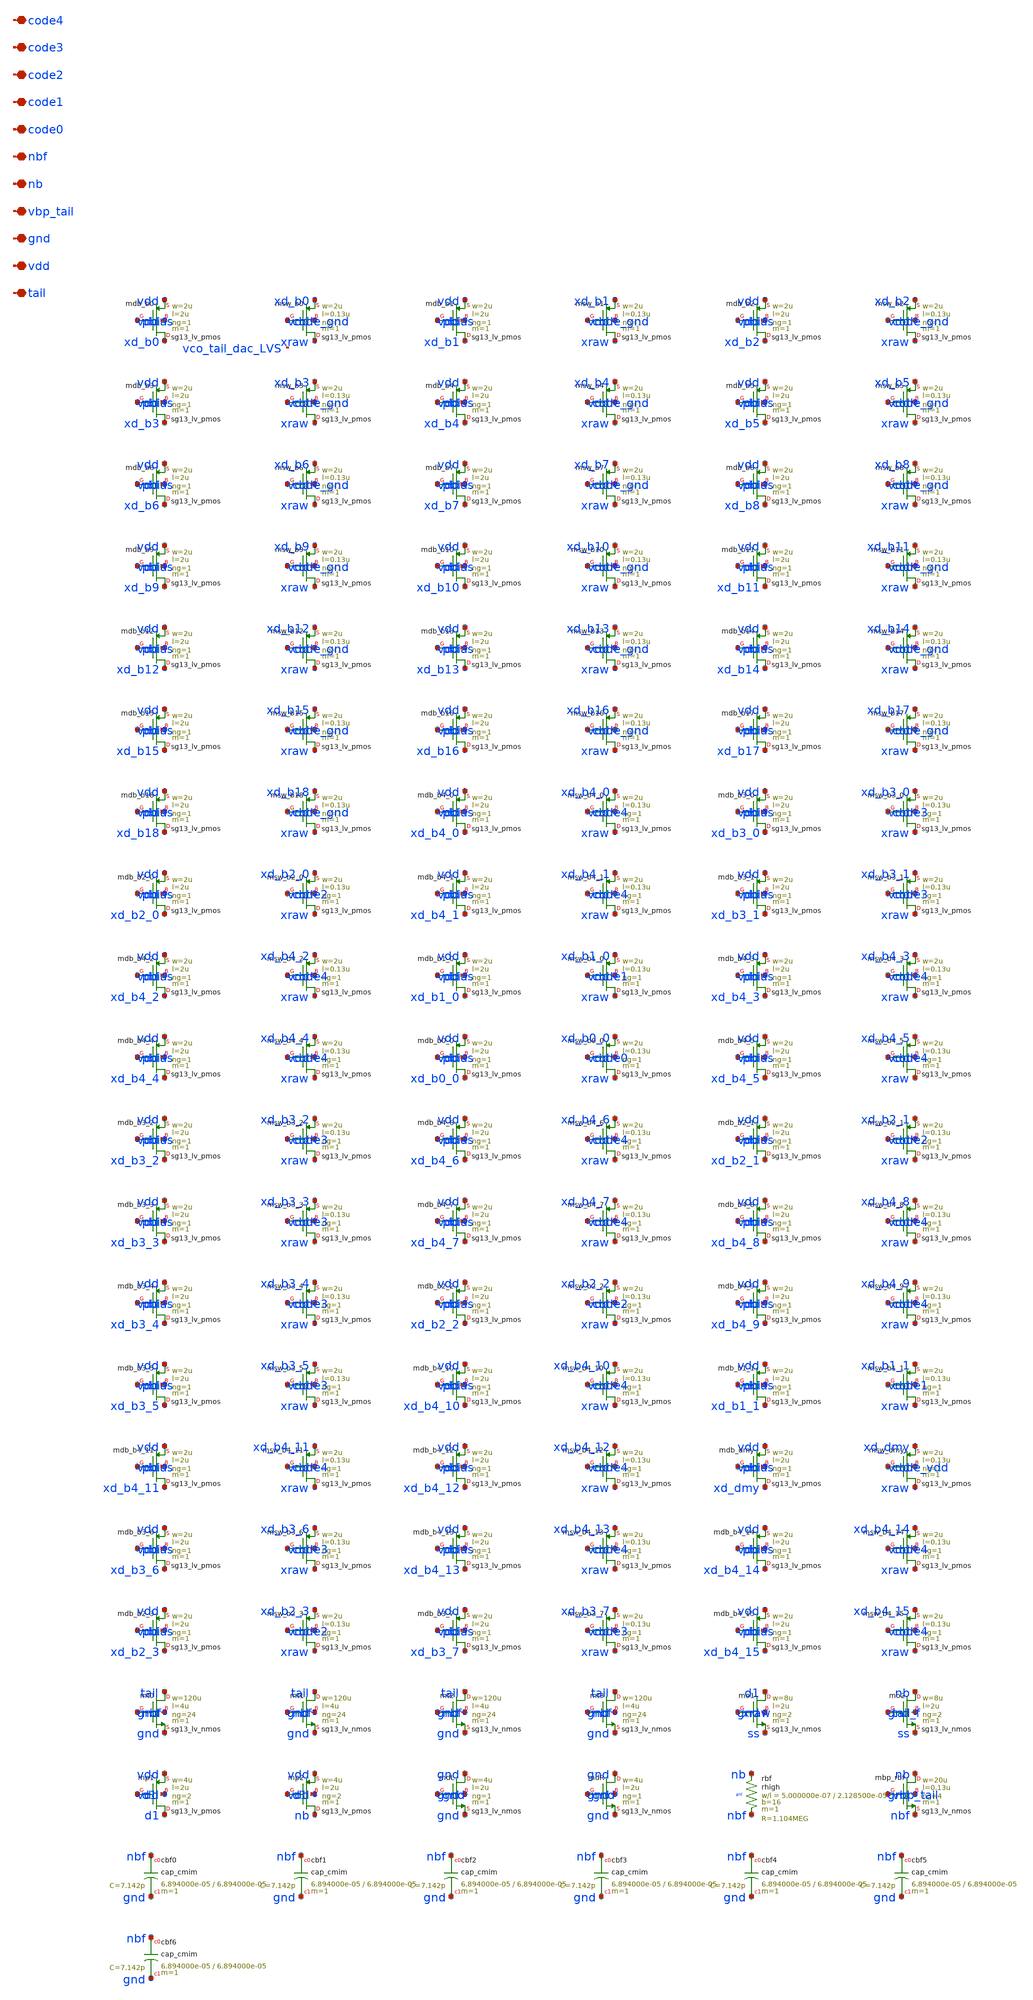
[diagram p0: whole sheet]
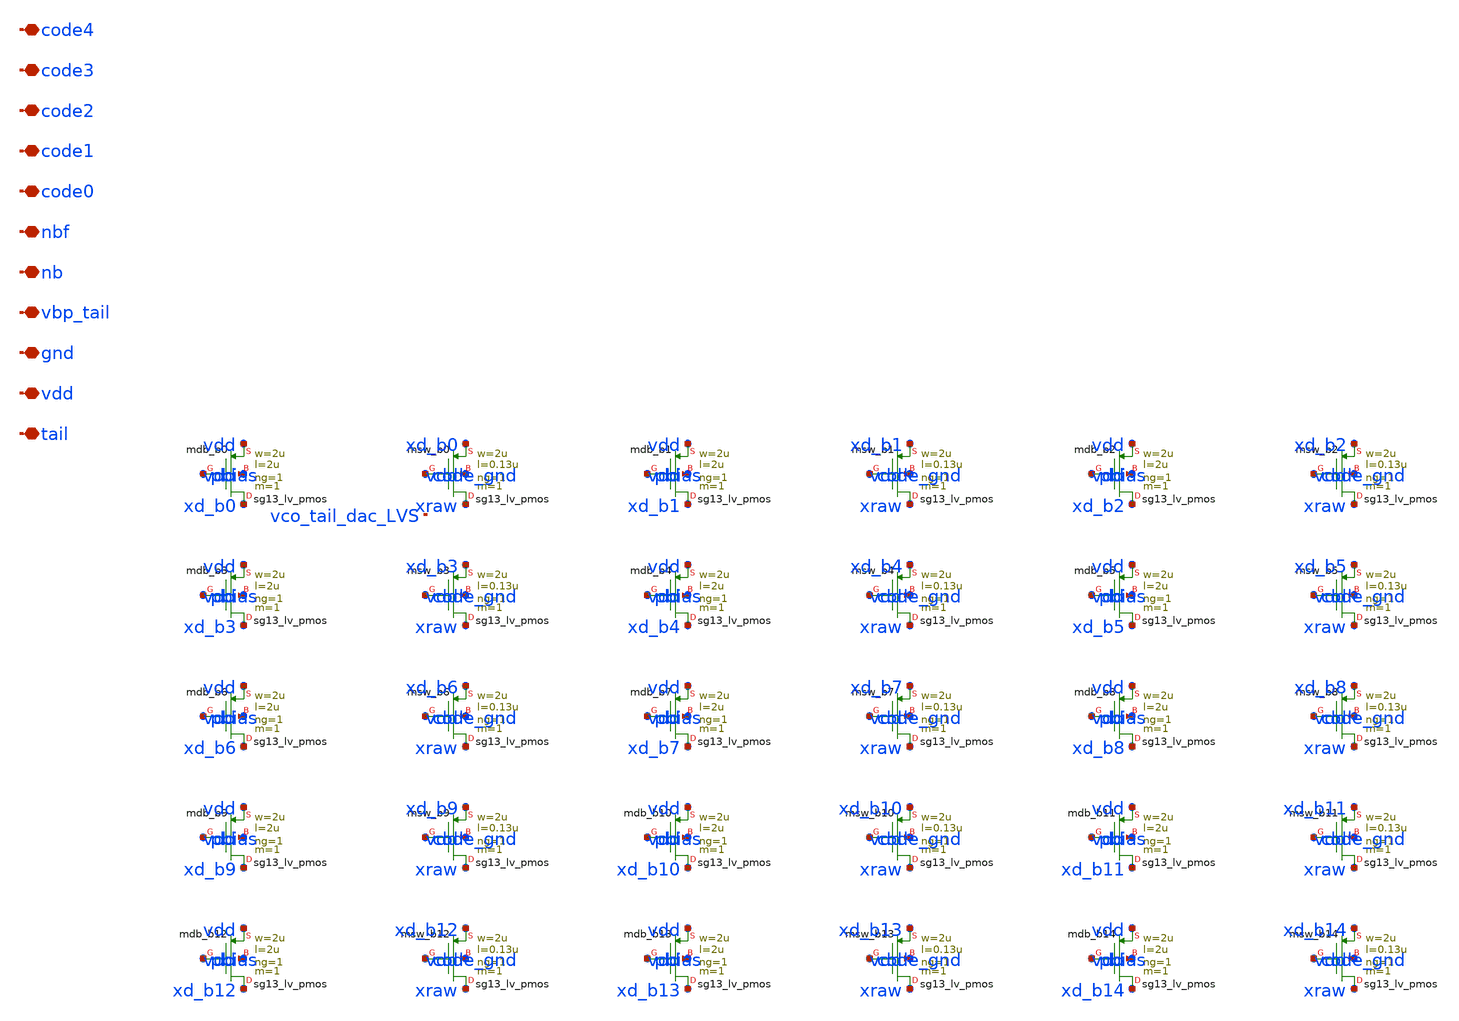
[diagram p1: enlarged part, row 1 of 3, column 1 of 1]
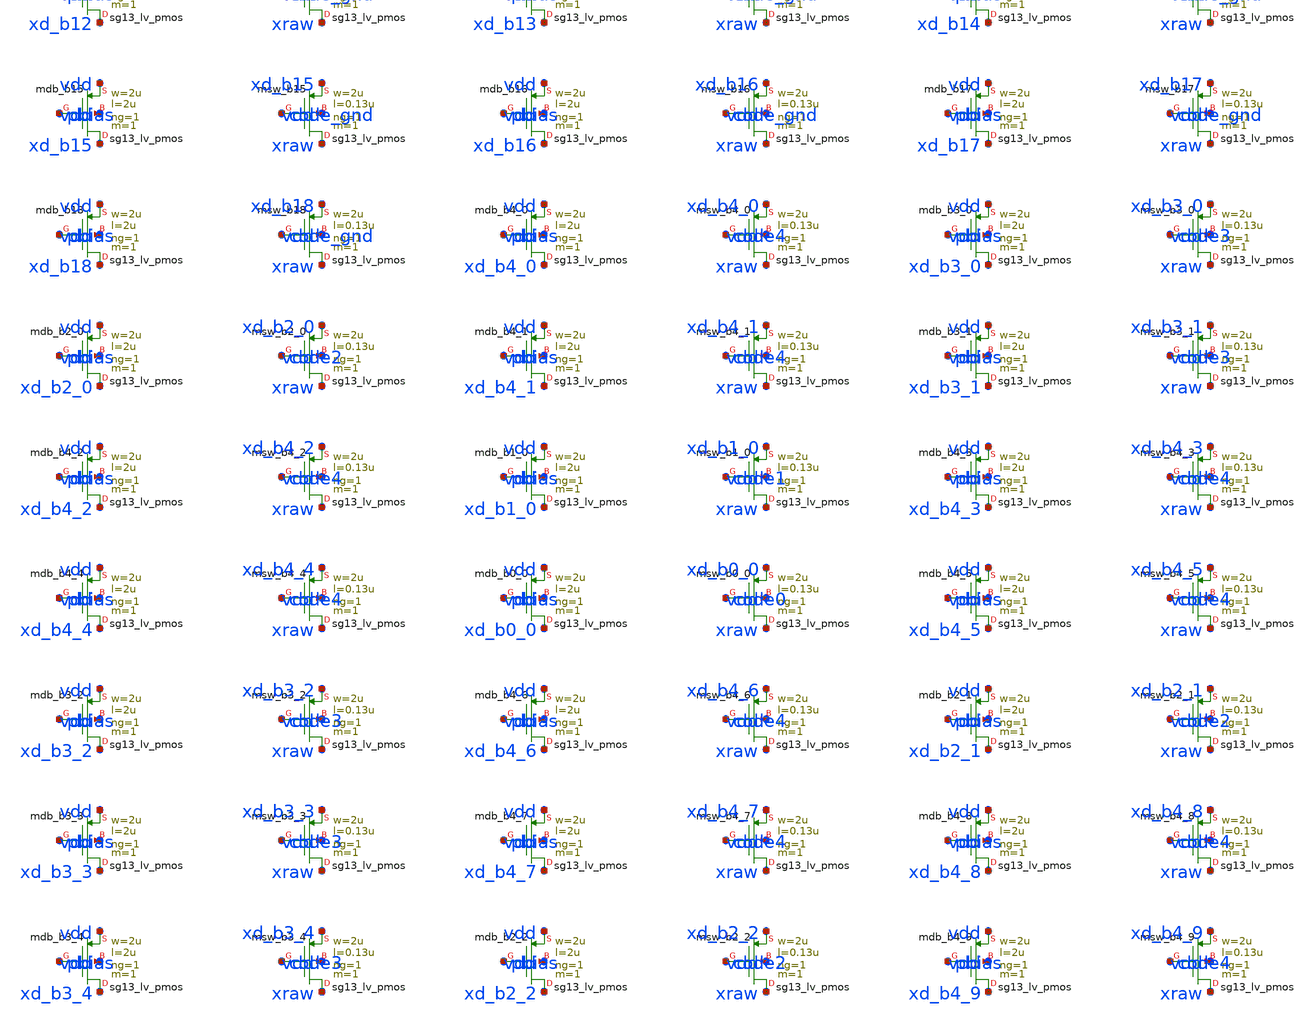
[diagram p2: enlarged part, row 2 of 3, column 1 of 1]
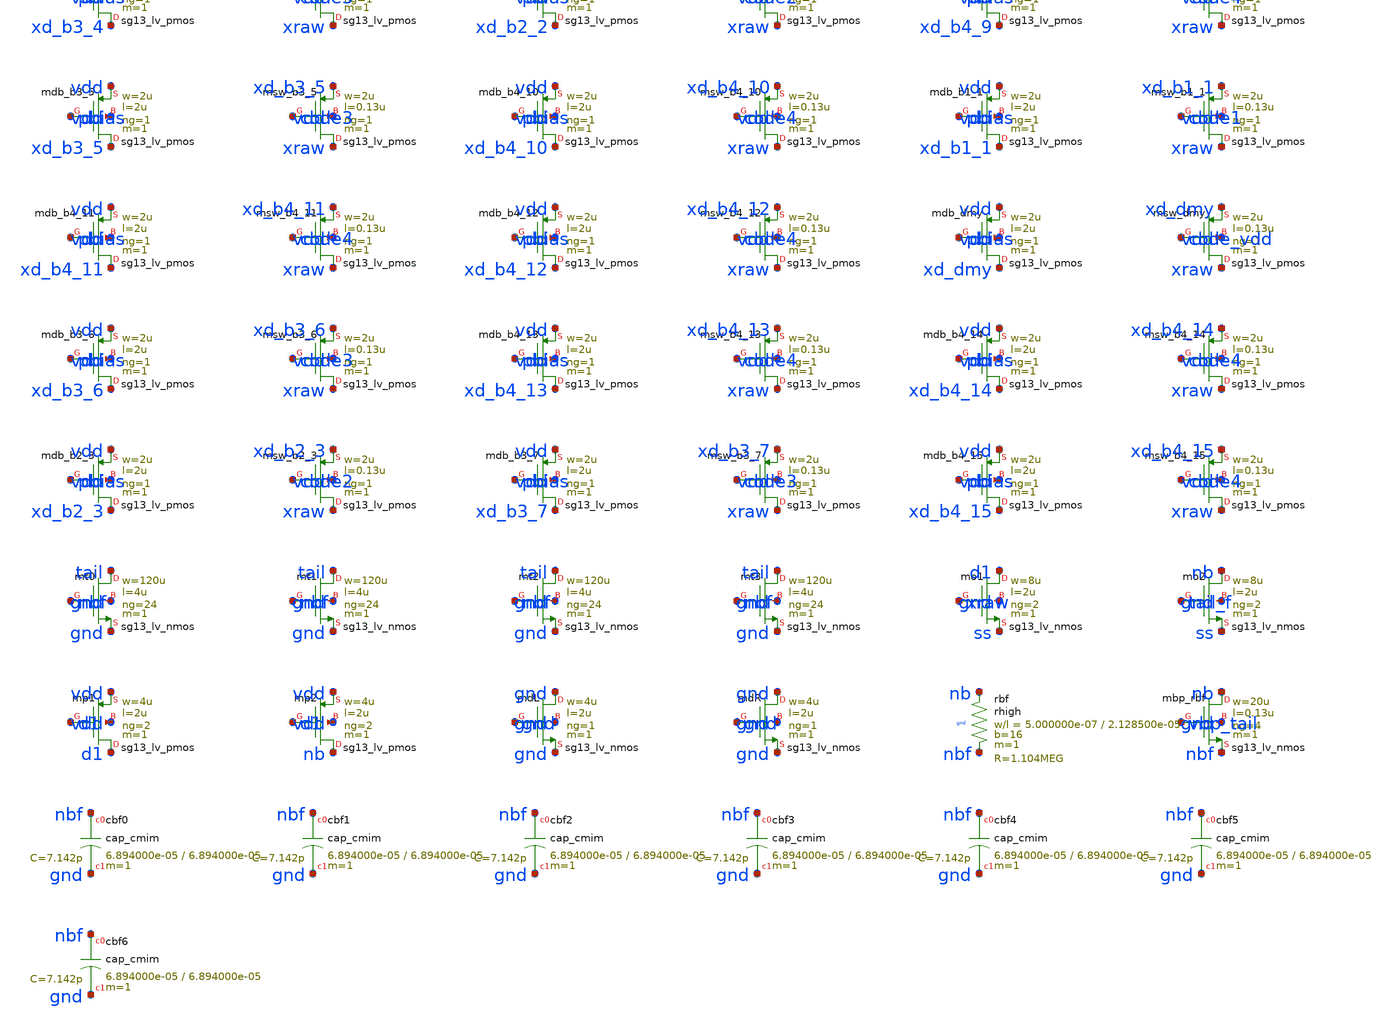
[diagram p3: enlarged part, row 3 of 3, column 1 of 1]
** sch_path: analog/vco/sch/vco_tail_dac.sch
**.subckt vco_tail_dac tail vdd gnd vbp_tail nb nbf code0 code1 code2 code3 code4
*.iopin tail
*.iopin vdd
*.iopin gnd
*.iopin vbp_tail
*.iopin nb
*.iopin nbf
*.iopin code0
*.iopin code1
*.iopin code2
*.iopin code3
*.iopin code4
Xmdb_b0 xd_b0 pbias vdd vdd sg13_lv_pmos w=2u l=2u ng=1 m=1 mm_ok=1
Xmsw_b0 xraw code_gnd xd_b0 vdd sg13_lv_pmos w=2u l=0.13u ng=1 m=1 mm_ok=1
Xmdb_b1 xd_b1 pbias vdd vdd sg13_lv_pmos w=2u l=2u ng=1 m=1 mm_ok=1
Xmsw_b1 xraw code_gnd xd_b1 vdd sg13_lv_pmos w=2u l=0.13u ng=1 m=1 mm_ok=1
Xmdb_b2 xd_b2 pbias vdd vdd sg13_lv_pmos w=2u l=2u ng=1 m=1 mm_ok=1
Xmsw_b2 xraw code_gnd xd_b2 vdd sg13_lv_pmos w=2u l=0.13u ng=1 m=1 mm_ok=1
Xmdb_b3 xd_b3 pbias vdd vdd sg13_lv_pmos w=2u l=2u ng=1 m=1 mm_ok=1
Xmsw_b3 xraw code_gnd xd_b3 vdd sg13_lv_pmos w=2u l=0.13u ng=1 m=1 mm_ok=1
Xmdb_b4 xd_b4 pbias vdd vdd sg13_lv_pmos w=2u l=2u ng=1 m=1 mm_ok=1
Xmsw_b4 xraw code_gnd xd_b4 vdd sg13_lv_pmos w=2u l=0.13u ng=1 m=1 mm_ok=1
Xmdb_b5 xd_b5 pbias vdd vdd sg13_lv_pmos w=2u l=2u ng=1 m=1 mm_ok=1
Xmsw_b5 xraw code_gnd xd_b5 vdd sg13_lv_pmos w=2u l=0.13u ng=1 m=1 mm_ok=1
Xmdb_b6 xd_b6 pbias vdd vdd sg13_lv_pmos w=2u l=2u ng=1 m=1 mm_ok=1
Xmsw_b6 xraw code_gnd xd_b6 vdd sg13_lv_pmos w=2u l=0.13u ng=1 m=1 mm_ok=1
Xmdb_b7 xd_b7 pbias vdd vdd sg13_lv_pmos w=2u l=2u ng=1 m=1 mm_ok=1
Xmsw_b7 xraw code_gnd xd_b7 vdd sg13_lv_pmos w=2u l=0.13u ng=1 m=1 mm_ok=1
Xmdb_b8 xd_b8 pbias vdd vdd sg13_lv_pmos w=2u l=2u ng=1 m=1 mm_ok=1
Xmsw_b8 xraw code_gnd xd_b8 vdd sg13_lv_pmos w=2u l=0.13u ng=1 m=1 mm_ok=1
Xmdb_b9 xd_b9 pbias vdd vdd sg13_lv_pmos w=2u l=2u ng=1 m=1 mm_ok=1
Xmsw_b9 xraw code_gnd xd_b9 vdd sg13_lv_pmos w=2u l=0.13u ng=1 m=1 mm_ok=1
Xmdb_b10 xd_b10 pbias vdd vdd sg13_lv_pmos w=2u l=2u ng=1 m=1 mm_ok=1
Xmsw_b10 xraw code_gnd xd_b10 vdd sg13_lv_pmos w=2u l=0.13u ng=1 m=1 mm_ok=1
Xmdb_b11 xd_b11 pbias vdd vdd sg13_lv_pmos w=2u l=2u ng=1 m=1 mm_ok=1
Xmsw_b11 xraw code_gnd xd_b11 vdd sg13_lv_pmos w=2u l=0.13u ng=1 m=1 mm_ok=1
Xmdb_b12 xd_b12 pbias vdd vdd sg13_lv_pmos w=2u l=2u ng=1 m=1 mm_ok=1
Xmsw_b12 xraw code_gnd xd_b12 vdd sg13_lv_pmos w=2u l=0.13u ng=1 m=1 mm_ok=1
Xmdb_b13 xd_b13 pbias vdd vdd sg13_lv_pmos w=2u l=2u ng=1 m=1 mm_ok=1
Xmsw_b13 xraw code_gnd xd_b13 vdd sg13_lv_pmos w=2u l=0.13u ng=1 m=1 mm_ok=1
Xmdb_b14 xd_b14 pbias vdd vdd sg13_lv_pmos w=2u l=2u ng=1 m=1 mm_ok=1
Xmsw_b14 xraw code_gnd xd_b14 vdd sg13_lv_pmos w=2u l=0.13u ng=1 m=1 mm_ok=1
Xmdb_b15 xd_b15 pbias vdd vdd sg13_lv_pmos w=2u l=2u ng=1 m=1 mm_ok=1
Xmsw_b15 xraw code_gnd xd_b15 vdd sg13_lv_pmos w=2u l=0.13u ng=1 m=1 mm_ok=1
Xmdb_b16 xd_b16 pbias vdd vdd sg13_lv_pmos w=2u l=2u ng=1 m=1 mm_ok=1
Xmsw_b16 xraw code_gnd xd_b16 vdd sg13_lv_pmos w=2u l=0.13u ng=1 m=1 mm_ok=1
Xmdb_b17 xd_b17 pbias vdd vdd sg13_lv_pmos w=2u l=2u ng=1 m=1 mm_ok=1
Xmsw_b17 xraw code_gnd xd_b17 vdd sg13_lv_pmos w=2u l=0.13u ng=1 m=1 mm_ok=1
Xmdb_b18 xd_b18 pbias vdd vdd sg13_lv_pmos w=2u l=2u ng=1 m=1 mm_ok=1
Xmsw_b18 xraw code_gnd xd_b18 vdd sg13_lv_pmos w=2u l=0.13u ng=1 m=1 mm_ok=1
Xmdb_b4_0 xd_b4_0 pbias vdd vdd sg13_lv_pmos w=2u l=2u ng=1 m=1 mm_ok=1
Xmsw_b4_0 xraw code4 xd_b4_0 vdd sg13_lv_pmos w=2u l=0.13u ng=1 m=1 mm_ok=1
Xmdb_b3_0 xd_b3_0 pbias vdd vdd sg13_lv_pmos w=2u l=2u ng=1 m=1 mm_ok=1
Xmsw_b3_0 xraw code3 xd_b3_0 vdd sg13_lv_pmos w=2u l=0.13u ng=1 m=1 mm_ok=1
Xmdb_b2_0 xd_b2_0 pbias vdd vdd sg13_lv_pmos w=2u l=2u ng=1 m=1 mm_ok=1
Xmsw_b2_0 xraw code2 xd_b2_0 vdd sg13_lv_pmos w=2u l=0.13u ng=1 m=1 mm_ok=1
Xmdb_b4_1 xd_b4_1 pbias vdd vdd sg13_lv_pmos w=2u l=2u ng=1 m=1 mm_ok=1
Xmsw_b4_1 xraw code4 xd_b4_1 vdd sg13_lv_pmos w=2u l=0.13u ng=1 m=1 mm_ok=1
Xmdb_b3_1 xd_b3_1 pbias vdd vdd sg13_lv_pmos w=2u l=2u ng=1 m=1 mm_ok=1
Xmsw_b3_1 xraw code3 xd_b3_1 vdd sg13_lv_pmos w=2u l=0.13u ng=1 m=1 mm_ok=1
Xmdb_b4_2 xd_b4_2 pbias vdd vdd sg13_lv_pmos w=2u l=2u ng=1 m=1 mm_ok=1
Xmsw_b4_2 xraw code4 xd_b4_2 vdd sg13_lv_pmos w=2u l=0.13u ng=1 m=1 mm_ok=1
Xmdb_b1_0 xd_b1_0 pbias vdd vdd sg13_lv_pmos w=2u l=2u ng=1 m=1 mm_ok=1
Xmsw_b1_0 xraw code1 xd_b1_0 vdd sg13_lv_pmos w=2u l=0.13u ng=1 m=1 mm_ok=1
Xmdb_b4_3 xd_b4_3 pbias vdd vdd sg13_lv_pmos w=2u l=2u ng=1 m=1 mm_ok=1
Xmsw_b4_3 xraw code4 xd_b4_3 vdd sg13_lv_pmos w=2u l=0.13u ng=1 m=1 mm_ok=1
Xmdb_b4_4 xd_b4_4 pbias vdd vdd sg13_lv_pmos w=2u l=2u ng=1 m=1 mm_ok=1
Xmsw_b4_4 xraw code4 xd_b4_4 vdd sg13_lv_pmos w=2u l=0.13u ng=1 m=1 mm_ok=1
Xmdb_b0_0 xd_b0_0 pbias vdd vdd sg13_lv_pmos w=2u l=2u ng=1 m=1 mm_ok=1
Xmsw_b0_0 xraw code0 xd_b0_0 vdd sg13_lv_pmos w=2u l=0.13u ng=1 m=1 mm_ok=1
Xmdb_b4_5 xd_b4_5 pbias vdd vdd sg13_lv_pmos w=2u l=2u ng=1 m=1 mm_ok=1
Xmsw_b4_5 xraw code4 xd_b4_5 vdd sg13_lv_pmos w=2u l=0.13u ng=1 m=1 mm_ok=1
Xmdb_b3_2 xd_b3_2 pbias vdd vdd sg13_lv_pmos w=2u l=2u ng=1 m=1 mm_ok=1
Xmsw_b3_2 xraw code3 xd_b3_2 vdd sg13_lv_pmos w=2u l=0.13u ng=1 m=1 mm_ok=1
Xmdb_b4_6 xd_b4_6 pbias vdd vdd sg13_lv_pmos w=2u l=2u ng=1 m=1 mm_ok=1
Xmsw_b4_6 xraw code4 xd_b4_6 vdd sg13_lv_pmos w=2u l=0.13u ng=1 m=1 mm_ok=1
Xmdb_b2_1 xd_b2_1 pbias vdd vdd sg13_lv_pmos w=2u l=2u ng=1 m=1 mm_ok=1
Xmsw_b2_1 xraw code2 xd_b2_1 vdd sg13_lv_pmos w=2u l=0.13u ng=1 m=1 mm_ok=1
Xmdb_b3_3 xd_b3_3 pbias vdd vdd sg13_lv_pmos w=2u l=2u ng=1 m=1 mm_ok=1
Xmsw_b3_3 xraw code3 xd_b3_3 vdd sg13_lv_pmos w=2u l=0.13u ng=1 m=1 mm_ok=1
Xmdb_b4_7 xd_b4_7 pbias vdd vdd sg13_lv_pmos w=2u l=2u ng=1 m=1 mm_ok=1
Xmsw_b4_7 xraw code4 xd_b4_7 vdd sg13_lv_pmos w=2u l=0.13u ng=1 m=1 mm_ok=1
Xmdb_b4_8 xd_b4_8 pbias vdd vdd sg13_lv_pmos w=2u l=2u ng=1 m=1 mm_ok=1
Xmsw_b4_8 xraw code4 xd_b4_8 vdd sg13_lv_pmos w=2u l=0.13u ng=1 m=1 mm_ok=1
Xmdb_b3_4 xd_b3_4 pbias vdd vdd sg13_lv_pmos w=2u l=2u ng=1 m=1 mm_ok=1
Xmsw_b3_4 xraw code3 xd_b3_4 vdd sg13_lv_pmos w=2u l=0.13u ng=1 m=1 mm_ok=1
Xmdb_b2_2 xd_b2_2 pbias vdd vdd sg13_lv_pmos w=2u l=2u ng=1 m=1 mm_ok=1
Xmsw_b2_2 xraw code2 xd_b2_2 vdd sg13_lv_pmos w=2u l=0.13u ng=1 m=1 mm_ok=1
Xmdb_b4_9 xd_b4_9 pbias vdd vdd sg13_lv_pmos w=2u l=2u ng=1 m=1 mm_ok=1
Xmsw_b4_9 xraw code4 xd_b4_9 vdd sg13_lv_pmos w=2u l=0.13u ng=1 m=1 mm_ok=1
Xmdb_b3_5 xd_b3_5 pbias vdd vdd sg13_lv_pmos w=2u l=2u ng=1 m=1 mm_ok=1
Xmsw_b3_5 xraw code3 xd_b3_5 vdd sg13_lv_pmos w=2u l=0.13u ng=1 m=1 mm_ok=1
Xmdb_b4_10 xd_b4_10 pbias vdd vdd sg13_lv_pmos w=2u l=2u ng=1 m=1 mm_ok=1
Xmsw_b4_10 xraw code4 xd_b4_10 vdd sg13_lv_pmos w=2u l=0.13u ng=1 m=1 mm_ok=1
Xmdb_b1_1 xd_b1_1 pbias vdd vdd sg13_lv_pmos w=2u l=2u ng=1 m=1 mm_ok=1
Xmsw_b1_1 xraw code1 xd_b1_1 vdd sg13_lv_pmos w=2u l=0.13u ng=1 m=1 mm_ok=1
Xmdb_b4_11 xd_b4_11 pbias vdd vdd sg13_lv_pmos w=2u l=2u ng=1 m=1 mm_ok=1
Xmsw_b4_11 xraw code4 xd_b4_11 vdd sg13_lv_pmos w=2u l=0.13u ng=1 m=1 mm_ok=1
Xmdb_b4_12 xd_b4_12 pbias vdd vdd sg13_lv_pmos w=2u l=2u ng=1 m=1 mm_ok=1
Xmsw_b4_12 xraw code4 xd_b4_12 vdd sg13_lv_pmos w=2u l=0.13u ng=1 m=1 mm_ok=1
Xmdb_dmy xd_dmy pbias vdd vdd sg13_lv_pmos w=2u l=2u ng=1 m=1 mm_ok=1
Xmsw_dmy xraw code_vdd xd_dmy vdd sg13_lv_pmos w=2u l=0.13u ng=1 m=1 mm_ok=1
Xmdb_b3_6 xd_b3_6 pbias vdd vdd sg13_lv_pmos w=2u l=2u ng=1 m=1 mm_ok=1
Xmsw_b3_6 xraw code3 xd_b3_6 vdd sg13_lv_pmos w=2u l=0.13u ng=1 m=1 mm_ok=1
Xmdb_b4_13 xd_b4_13 pbias vdd vdd sg13_lv_pmos w=2u l=2u ng=1 m=1 mm_ok=1
Xmsw_b4_13 xraw code4 xd_b4_13 vdd sg13_lv_pmos w=2u l=0.13u ng=1 m=1 mm_ok=1
Xmdb_b4_14 xd_b4_14 pbias vdd vdd sg13_lv_pmos w=2u l=2u ng=1 m=1 mm_ok=1
Xmsw_b4_14 xraw code4 xd_b4_14 vdd sg13_lv_pmos w=2u l=0.13u ng=1 m=1 mm_ok=1
Xmdb_b2_3 xd_b2_3 pbias vdd vdd sg13_lv_pmos w=2u l=2u ng=1 m=1 mm_ok=1
Xmsw_b2_3 xraw code2 xd_b2_3 vdd sg13_lv_pmos w=2u l=0.13u ng=1 m=1 mm_ok=1
Xmdb_b3_7 xd_b3_7 pbias vdd vdd sg13_lv_pmos w=2u l=2u ng=1 m=1 mm_ok=1
Xmsw_b3_7 xraw code3 xd_b3_7 vdd sg13_lv_pmos w=2u l=0.13u ng=1 m=1 mm_ok=1
Xmdb_b4_15 xd_b4_15 pbias vdd vdd sg13_lv_pmos w=2u l=2u ng=1 m=1 mm_ok=1
Xmsw_b4_15 xraw code4 xd_b4_15 vdd sg13_lv_pmos w=2u l=0.13u ng=1 m=1 mm_ok=1
Xmt0 tail nbf gnd gnd sg13_lv_nmos w=120u l=4u ng=24 m=1 mm_ok=1
Xmt1 tail nbf gnd gnd sg13_lv_nmos w=120u l=4u ng=24 m=1 mm_ok=1
Xmt2 tail nbf gnd gnd sg13_lv_nmos w=120u l=4u ng=24 m=1 mm_ok=1
Xmt3 tail nbf gnd gnd sg13_lv_nmos w=120u l=4u ng=24 m=1 mm_ok=1
Xmo1 d1 xraw ss gnd sg13_lv_nmos w=8u l=2u ng=2 m=1 mm_ok=1
Xmo2 nb tail_f ss gnd sg13_lv_nmos w=8u l=2u ng=2 m=1 mm_ok=1
Xmp1 d1 d1 vdd vdd sg13_lv_pmos w=4u l=2u ng=2 m=1 mm_ok=1
Xmp2 nb d1 vdd vdd sg13_lv_pmos w=4u l=2u ng=2 m=1 mm_ok=1
XmdL gnd gnd gnd gnd sg13_lv_nmos w=4u l=2u ng=1 m=1 mm_ok=1
XmdR gnd gnd gnd gnd sg13_lv_nmos w=4u l=2u ng=1 m=1 mm_ok=1
Xrbf nb nbf gnd rhigh w=5.000000e-07 l=2.128500e-05 m=1 b=16 mm_ok=1
Xmbp_rbf nb vbp_tail nbf gnd sg13_lv_nmos w=20u l=0.13u ng=4 m=1 mm_ok=1
Xcbf0 nbf gnd cap_cmim w=6.894000e-05 l=6.894000e-05 m=1 mm_ok=1
Xcbf1 nbf gnd cap_cmim w=6.894000e-05 l=6.894000e-05 m=1 mm_ok=1
Xcbf2 nbf gnd cap_cmim w=6.894000e-05 l=6.894000e-05 m=1 mm_ok=1
Xcbf3 nbf gnd cap_cmim w=6.894000e-05 l=6.894000e-05 m=1 mm_ok=1
Xcbf4 nbf gnd cap_cmim w=6.894000e-05 l=6.894000e-05 m=1 mm_ok=1
Xcbf5 nbf gnd cap_cmim w=6.894000e-05 l=6.894000e-05 m=1 mm_ok=1
Xcbf6 nbf gnd cap_cmim w=6.894000e-05 l=6.894000e-05 m=1 mm_ok=1
**.ends
.end
